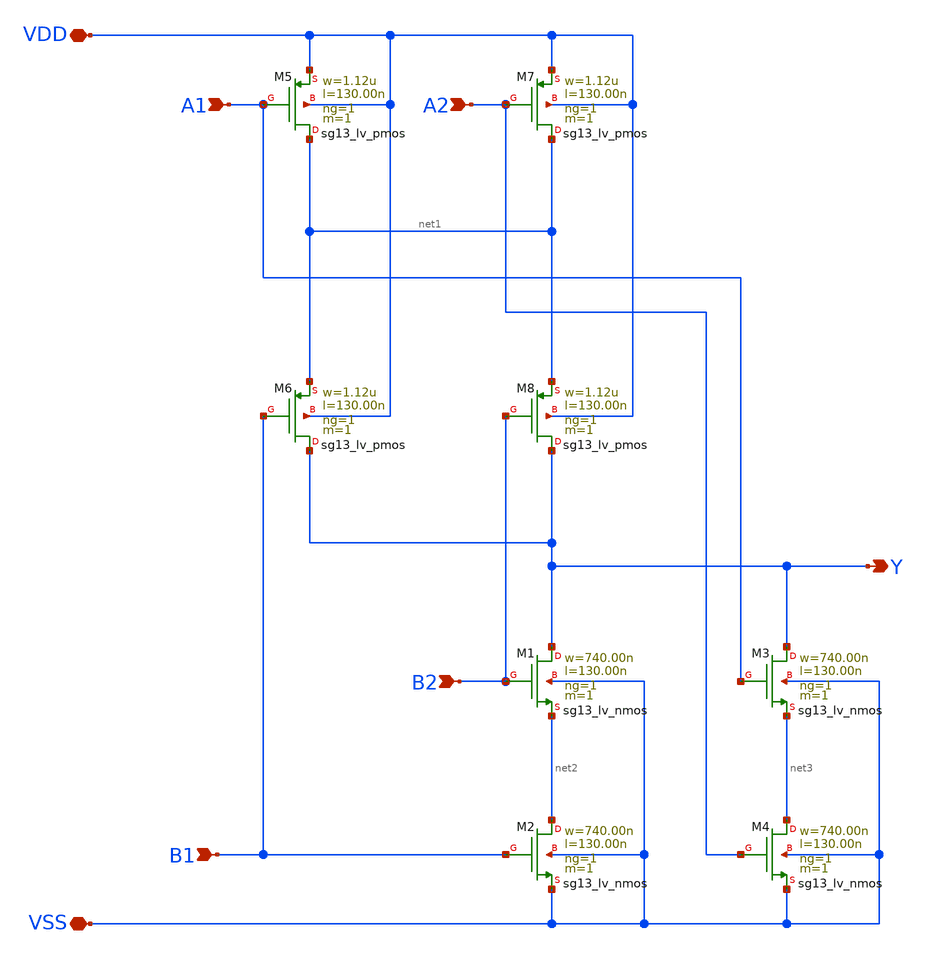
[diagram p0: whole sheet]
** sch_path: ihp-sg13g2/libs.tech/xschem/sg13g2_stdcells/sg13g2_a22oi_1.sch
**.subckt sg13g2_a22oi_1 A1 A2 B1 Y VDD VSS B2
*.ipin A1
*.ipin A2
*.ipin B1
*.opin Y
*.iopin VDD
*.iopin VSS
*.ipin B2
XM1 Y B2 net2 VSS sg13_lv_nmos w=740.00n l=130.00n ng=1 m=1 mm_ok=1
XM2 net2 B1 VSS VSS sg13_lv_nmos w=740.00n l=130.00n ng=1 m=1 mm_ok=1
XM3 Y A1 net3 VSS sg13_lv_nmos w=740.00n l=130.00n ng=1 m=1 mm_ok=1
XM4 net3 A2 VSS VSS sg13_lv_nmos w=740.00n l=130.00n ng=1 m=1 mm_ok=1
XM5 net1 A1 VDD VDD sg13_lv_pmos w=1.12u l=130.00n ng=1 m=1 mm_ok=1
XM6 Y B1 net1 VDD sg13_lv_pmos w=1.12u l=130.00n ng=1 m=1 mm_ok=1
XM7 net1 A2 VDD VDD sg13_lv_pmos w=1.12u l=130.00n ng=1 m=1 mm_ok=1
XM8 Y B2 net1 VDD sg13_lv_pmos w=1.12u l=130.00n ng=1 m=1 mm_ok=1
**.ends
.end
